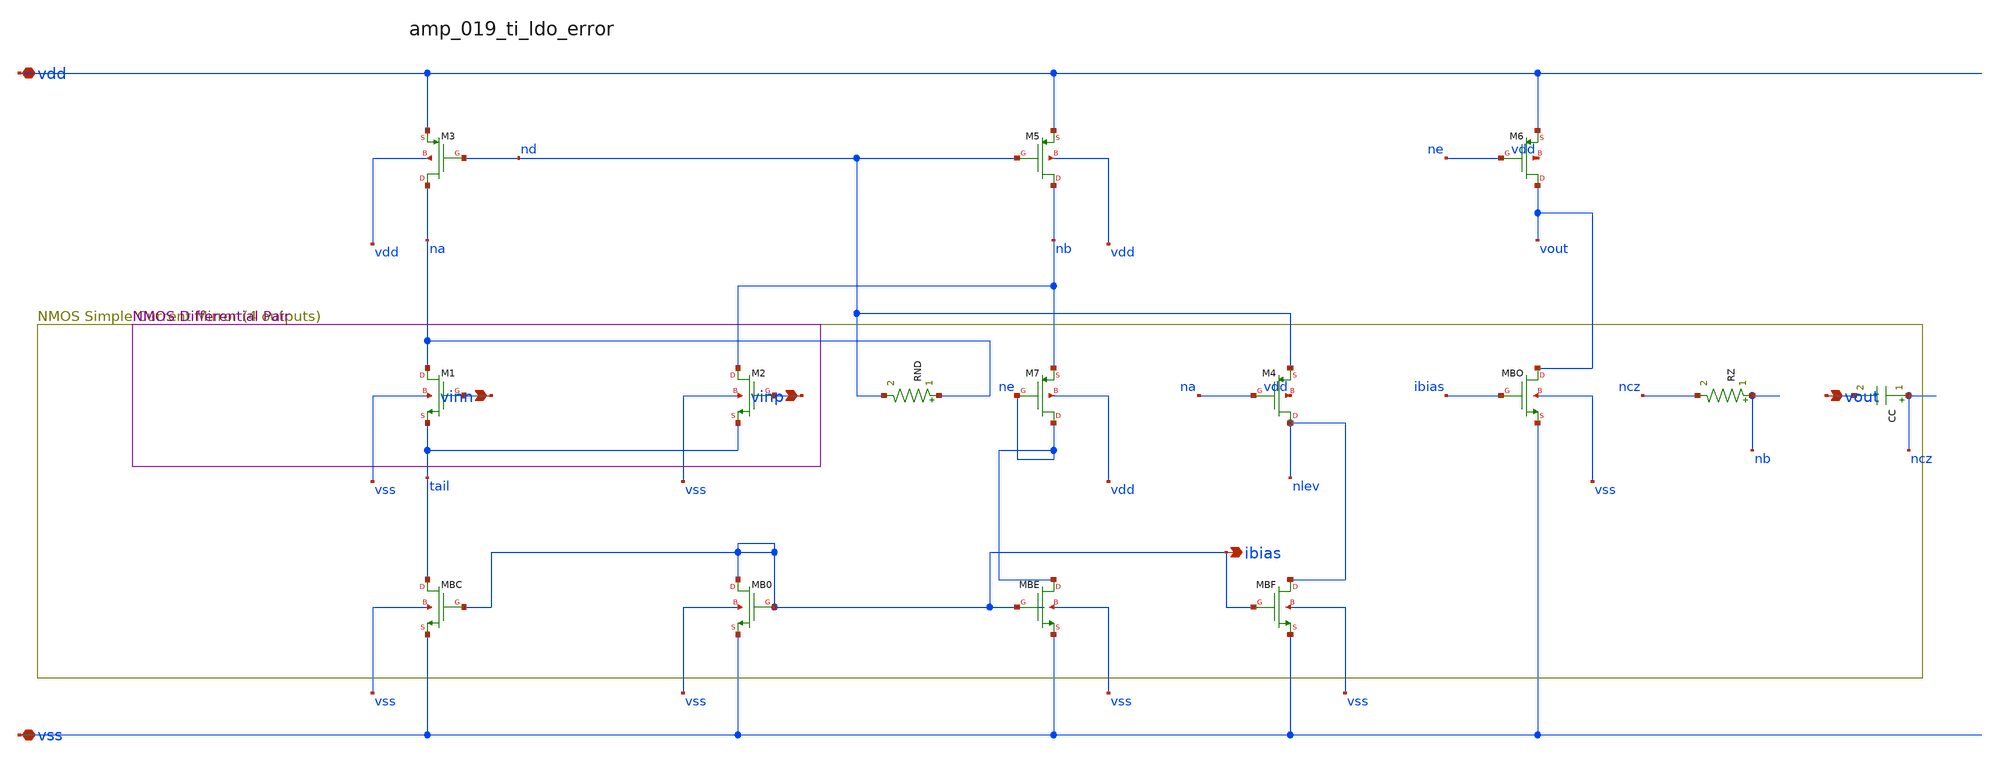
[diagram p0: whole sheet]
** sch_path: analog-db/raw/amp_019_ti_ldo_error/amp_019_ti_ldo_error_annotated.sch
**.subckt amp_019_ti_ldo_error_annotated vinn vinp vdd vss vout ibias
*.ipin vinn
*.ipin vinp
*.iopin vdd
*.iopin vss
*.opin vout
*.opin ibias
CC ncz vout 'c_comp' m=1
RND na nd 'r_nd' m=1
RZ nb ncz 'r_z' m=1
XM1 na vinn tail vss sg13_hv_nmos w=x_dut_xm1_w l=x_dut_xm1_l ng=1 m=1
XM2 nb vinp tail vss sg13_hv_nmos w=x_dut_xm2_w l=x_dut_xm2_l ng=1 m=1
XM3 na nd vdd vdd sg13_hv_pmos w=x_dut_xm3_w l=x_dut_xm3_l ng=1 m=1
XM4 nlev na nd vdd sg13_hv_pmos w=x_dut_xm4_w l=x_dut_xm4_l ng=1 m=1
XM5 nb nd vdd vdd sg13_hv_pmos w=x_dut_xm5_w l=x_dut_xm5_l ng=1 m=1
XM6 vout ne vdd vdd sg13_hv_pmos w=x_dut_xm6_w l=x_dut_xm6_l ng=1 m=1
XM7 ne ne nb vdd sg13_hv_pmos w=x_dut_xm7_w l=x_dut_xm7_l ng=1 m=1
XMB0 ibias ibias vss vss sg13_hv_nmos w=x_dut_xmb0_w l=x_dut_xmb0_l ng=1 m=1
XMBC tail ibias vss vss sg13_hv_nmos w=x_dut_xmbc_w l=x_dut_xmbc_l ng=1 m=x_dut_xmbc_m
XMBE ne ibias vss vss sg13_hv_nmos w=x_dut_xmbe_w l=x_dut_xmbe_l ng=1 m=1
XMBF nlev ibias vss vss sg13_hv_nmos w=x_dut_xmbf_w l=x_dut_xmbf_l ng=1 m=1
XMBO vout ibias vss vss sg13_hv_nmos w=x_dut_xmbo_w l=x_dut_xmbo_l ng=1 m=x_dut_xmbo_m
**.ends
.end
